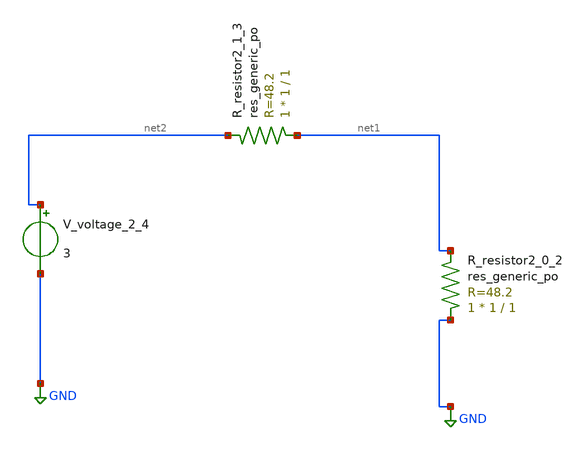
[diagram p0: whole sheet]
** sch_path: schematics/AMSNet/457.sch
**.subckt 457
XR_resistor2_0_2 GND net1 sky130_fd_pr__res_generic_po W=1 L=1 m=1
XR_resistor2_1_3 net1 net2 sky130_fd_pr__res_generic_po W=1 L=1 m=1
V_voltage_2_4 net2 GND 3
**.ends
.GLOBAL GND
.end
